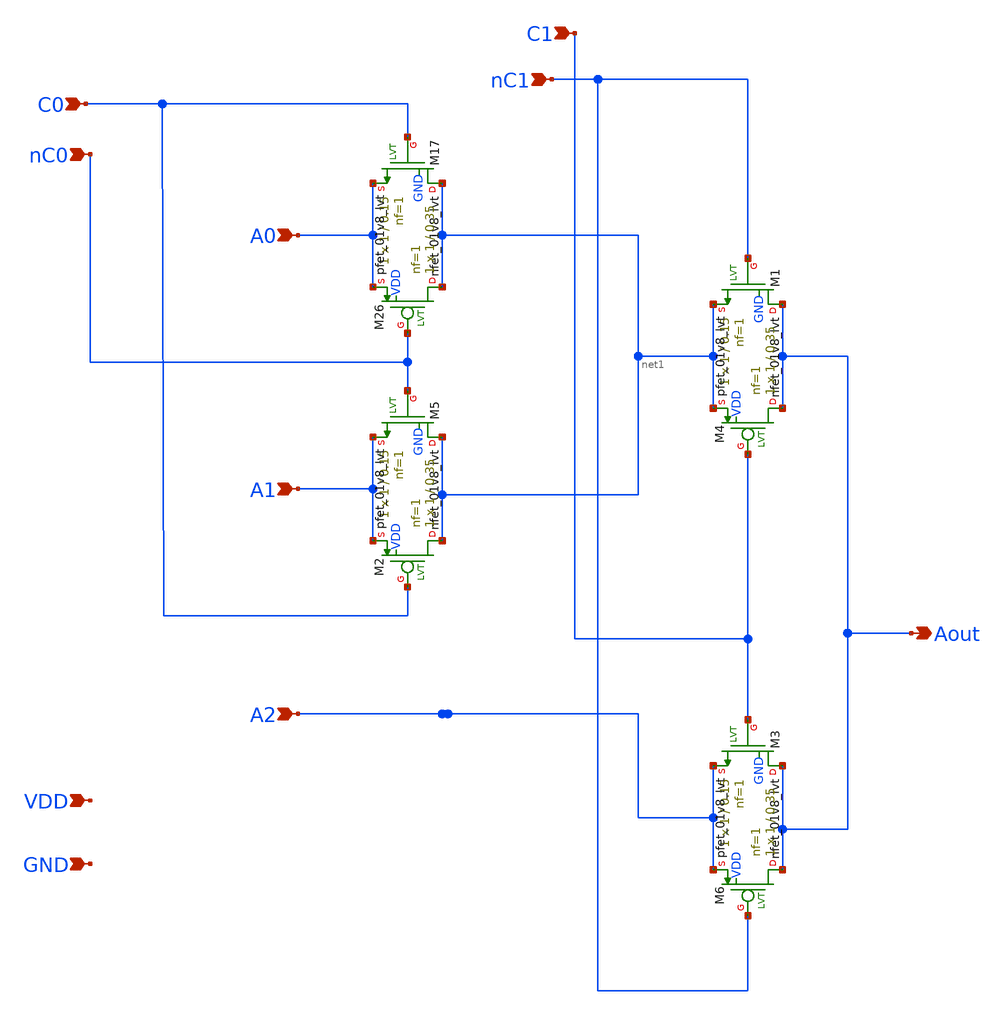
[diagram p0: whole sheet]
** sch_path: Analog_Mux.sch
**.subckt Analog_Mux C0 C1 A0 A2 A1 nC0 nC1 Aout VDD GND
*.ipin C0
*.ipin C1
*.ipin A0
*.ipin A2
*.ipin A1
*.ipin nC0
*.ipin nC1
*.opin Aout
*.ipin VDD
*.ipin GND
XM17 net1 C0 A0 GND sky130_fd_pr__nfet_01v8_lvt L=0.15 W=1 nf=1 ad='int((1 + 1)/2) * 1 / 1 * 0.29' as='int((1 + 2)/2) * 1 / 1 * 0.29'
+ pd='2*int((1 + 1)/2) * (1 / 1 + 0.29)' ps='2*int((1 + 2)/2) * (1 / 1 + 0.29)' nrd='0.29 / 1 ' nrs='0.29 / 1 '
+ sa=0 sb=0 sd=0 mult=1 m=1
XM1 Aout nC1 net1 GND sky130_fd_pr__nfet_01v8_lvt L=0.15 W=1 nf=1 ad='int((1 + 1)/2) * 1 / 1 * 0.29'
+ as='int((1 + 2)/2) * 1 / 1 * 0.29' pd='2*int((1 + 1)/2) * (1 / 1 + 0.29)' ps='2*int((1 + 2)/2) * (1 / 1 + 0.29)'
+ nrd='0.29 / 1 ' nrs='0.29 / 1 ' sa=0 sb=0 sd=0 mult=1 m=1
XM3 Aout C1 A2 GND sky130_fd_pr__nfet_01v8_lvt L=0.15 W=1 nf=1 ad='int((1 + 1)/2) * 1 / 1 * 0.29' as='int((1 + 2)/2) * 1 / 1 * 0.29'
+ pd='2*int((1 + 1)/2) * (1 / 1 + 0.29)' ps='2*int((1 + 2)/2) * (1 / 1 + 0.29)' nrd='0.29 / 1 ' nrs='0.29 / 1 '
+ sa=0 sb=0 sd=0 mult=1 m=1
XM5 net1 nC0 A1 GND sky130_fd_pr__nfet_01v8_lvt L=0.15 W=1 nf=1 ad='int((1 + 1)/2) * 1 / 1 * 0.29' as='int((1 + 2)/2) * 1 / 1 * 0.29'
+ pd='2*int((1 + 1)/2) * (1 / 1 + 0.29)' ps='2*int((1 + 2)/2) * (1 / 1 + 0.29)' nrd='0.29 / 1 ' nrs='0.29 / 1 '
+ sa=0 sb=0 sd=0 mult=1 m=1
XM26 net1 nC0 A0 VDD sky130_fd_pr__pfet_01v8_lvt L=0.35 W=1 nf=1 ad='int((1 + 1)/2) * 1 / 1 * 0.29' as='int((1 + 2)/2) * 1 / 1 * 0.29'
+ pd='2*int((1 + 1)/2) * (1 / 1 + 0.29)' ps='2*int((1 + 2)/2) * (1 / 1 + 0.29)' nrd='0.29 / 1 ' nrs='0.29 / 1 '
+ sa=0 sb=0 sd=0 mult=1 m=1
XM2 net1 C0 A1 VDD sky130_fd_pr__pfet_01v8_lvt L=0.35 W=1 nf=1 ad='int((1 + 1)/2) * 1 / 1 * 0.29' as='int((1 + 2)/2) * 1 / 1 * 0.29'
+ pd='2*int((1 + 1)/2) * (1 / 1 + 0.29)' ps='2*int((1 + 2)/2) * (1 / 1 + 0.29)' nrd='0.29 / 1 ' nrs='0.29 / 1 '
+ sa=0 sb=0 sd=0 mult=1 m=1
XM4 Aout C1 net1 VDD sky130_fd_pr__pfet_01v8_lvt L=0.35 W=1 nf=1 ad='int((1 + 1)/2) * 1 / 1 * 0.29' as='int((1 + 2)/2) * 1 / 1 * 0.29'
+ pd='2*int((1 + 1)/2) * (1 / 1 + 0.29)' ps='2*int((1 + 2)/2) * (1 / 1 + 0.29)' nrd='0.29 / 1 ' nrs='0.29 / 1 '
+ sa=0 sb=0 sd=0 mult=1 m=1
XM6 Aout nC1 A2 VDD sky130_fd_pr__pfet_01v8_lvt L=0.35 W=1 nf=1 ad='int((1 + 1)/2) * 1 / 1 * 0.29' as='int((1 + 2)/2) * 1 / 1 * 0.29'
+ pd='2*int((1 + 1)/2) * (1 / 1 + 0.29)' ps='2*int((1 + 2)/2) * (1 / 1 + 0.29)' nrd='0.29 / 1 ' nrs='0.29 / 1 '
+ sa=0 sb=0 sd=0 mult=1 m=1
**.ends
.end
